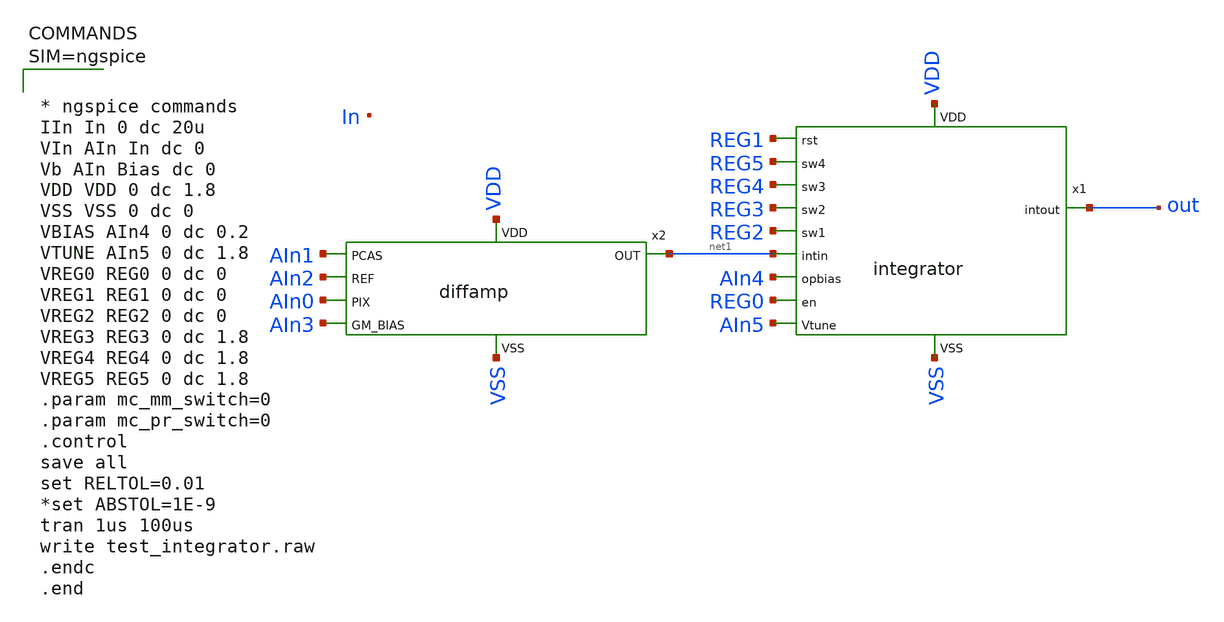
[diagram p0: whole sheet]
** sch_path: xschem/test_diffamp-integrator.sch
**.subckt test_diffamp-integrator
x1 REG3 REG2 net1 out AIn4 REG0 AIn5 REG1 REG5 REG4 VDD VSS integrator
x2 AIn1 net1 AIn2 AIn0 AIn3 VDD VSS diffamp
**** begin user architecture code

** opencircuitdesign pdks install
.lib $::SKYWATER_MODELS/sky130.lib.spice tt





* ngspice commands
IIn In 0 dc 20u
VIn AIn In dc 0
Vb AIn Bias dc 0
VDD VDD 0 dc 1.8
VSS VSS 0 dc 0
VBIAS AIn4 0 dc 0.2
VTUNE AIn5 0 dc 1.8
VREG0 REG0 0 dc 0
VREG1 REG1 0 dc 0
VREG2 REG2 0 dc 0
VREG3 REG3 0 dc 1.8
VREG4 REG4 0 dc 1.8
VREG5 REG5 0 dc 1.8
.param mc_mm_switch=0
.param mc_pr_switch=0
.control
save all
set RELTOL=0.01
*set ABSTOL=1E-9
tran 1us 100us
write test_integrator.raw
.endc
.end


**** end user architecture code
**.ends
.end
